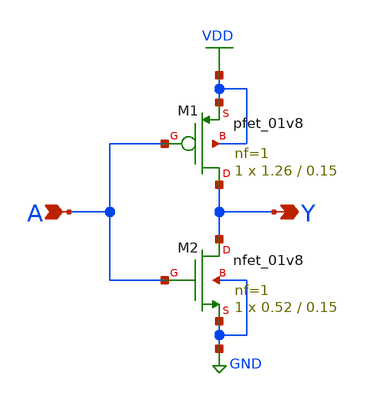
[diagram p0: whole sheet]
** sch_path: xschem/sim/inv.sch
**.subckt inv Y A
*.opin Y
*.ipin A
XM1 Y A VDD VDD sky130_fd_pr__pfet_01v8 L=0.15 W=1.26 nf=1 ad='int((nf+1)/2) * W/nf * 0.29' as='int((nf+2)/2) * W/nf * 0.29'
+ pd='2*int((nf+1)/2) * (W/nf + 0.29)' ps='2*int((nf+2)/2) * (W/nf + 0.29)' nrd='0.29 / W' nrs='0.29 / W'
+ sa=0 sb=0 sd=0 mult=1 m=1
XM2 Y A GND GND sky130_fd_pr__nfet_01v8 L=0.15 W=0.52 nf=1 ad='int((nf+1)/2) * W/nf * 0.29' as='int((nf+2)/2) * W/nf * 0.29'
+ pd='2*int((nf+1)/2) * (W/nf + 0.29)' ps='2*int((nf+2)/2) * (W/nf + 0.29)' nrd='0.29 / W' nrs='0.29 / W'
+ sa=0 sb=0 sd=0 mult=1 m=1
**** begin user architecture code

** opencircuitdesign pdks install
.lib $::SKYWATER_MODELS/sky130.lib.spice tt


**** end user architecture code
**.ends
.GLOBAL VDD
.GLOBAL GND
.end
